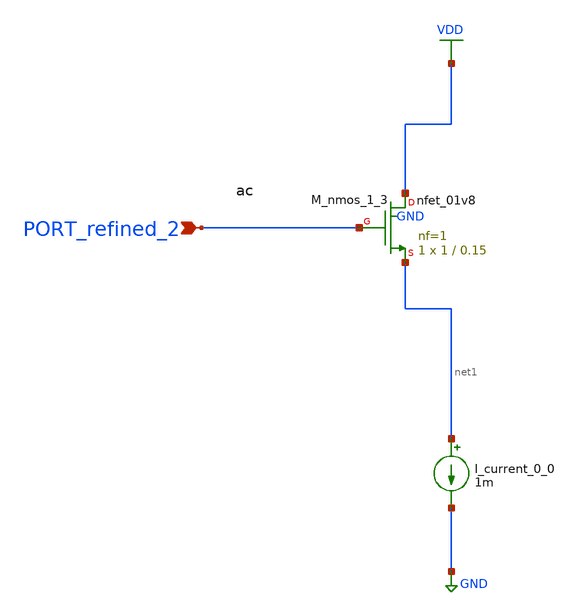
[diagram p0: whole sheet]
** sch_path: schematics/AMSNet/101.sch
**.subckt 101 PORT_refined_2
*.ipin PORT_refined_2
I_current_0_0 net1 GND 1m
XM_nmos_1_3 VDD PORT_refined_2 net1 GND sky130_fd_pr__nfet_01v8 L=0.15 W=1 nf=1 ad='int((1 + 1)/2) * 1 / 1 * 0.29'
+ as='int((1 + 2)/2) * 1 / 1 * 0.29' pd='2*int((1 + 1)/2) * (1 / 1 + 0.29)' ps='2*int((1 + 2)/2) * (1 / 1 + 0.29)'
+ nrd='0.29 / 1 ' nrs='0.29 / 1 ' sa=0 sb=0 sd=0 mult=1 m=1
**.ends
.GLOBAL GND
.GLOBAL VDD
.end
